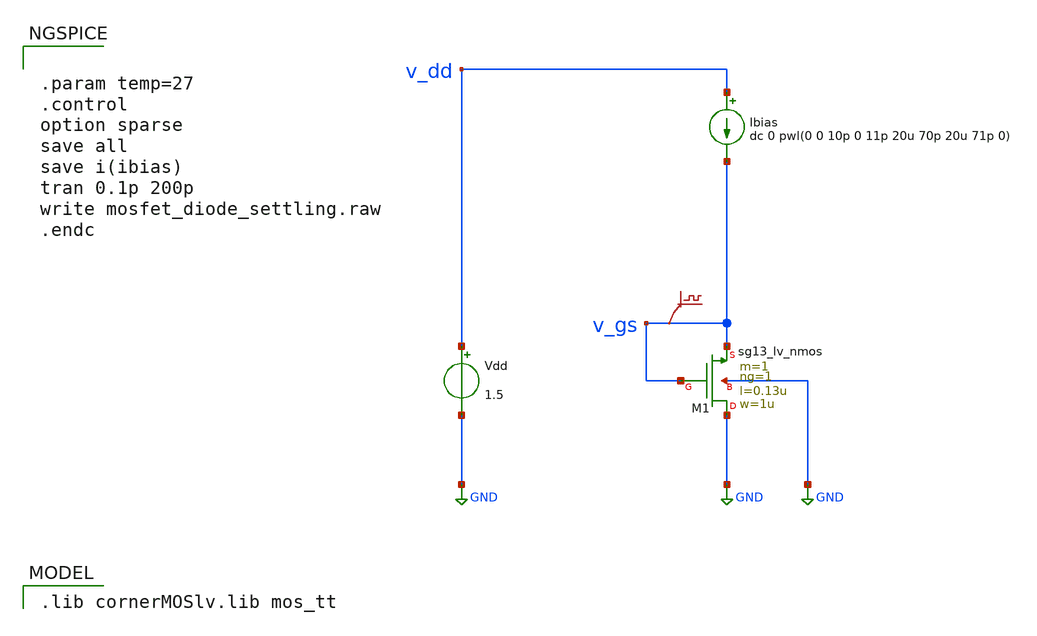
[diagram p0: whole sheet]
** sch_path: xschem/mosfet_diode_settling.sch
* Copyright 2024 Harald Pretl
**.subckt mosfet_diode_settling
Vdd v_dd GND 1.5
XM1 GND v_gs v_gs GND sg13_lv_nmos w=1u l=0.13u ng=1 m=1 mm_ok=1
Ibias v_dd v_gs dc 0 pwl(0 0 10p 0 11p 20u 70p 20u 71p 0)
.save v(v_gs)
**** begin user architecture code
 .lib cornerMOSlv.lib mos_tt



.param temp=27
.control
option sparse
save all
save i(ibias)
tran 0.1p 200p
write mosfet_diode_settling.raw
.endc


**** end user architecture code
**.ends
.GLOBAL GND
.end
